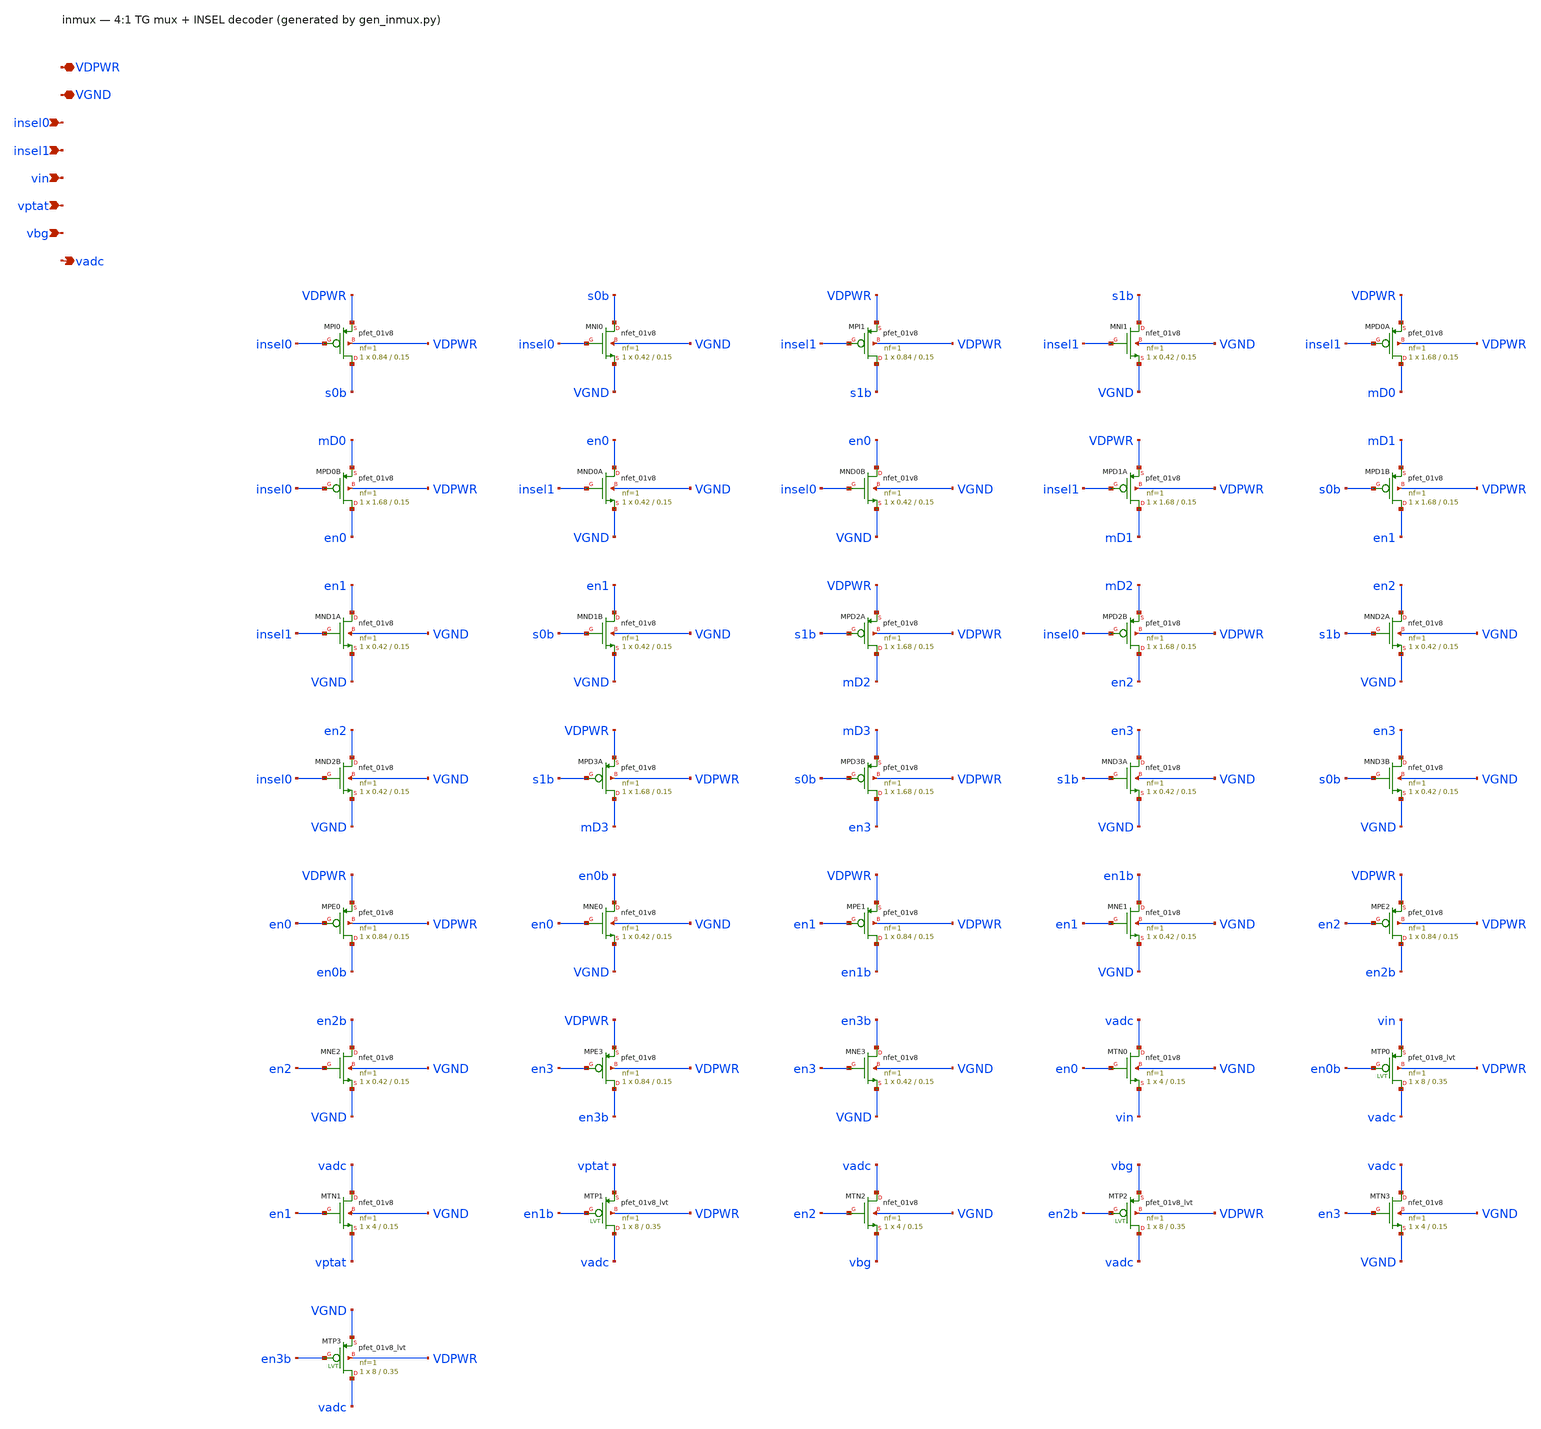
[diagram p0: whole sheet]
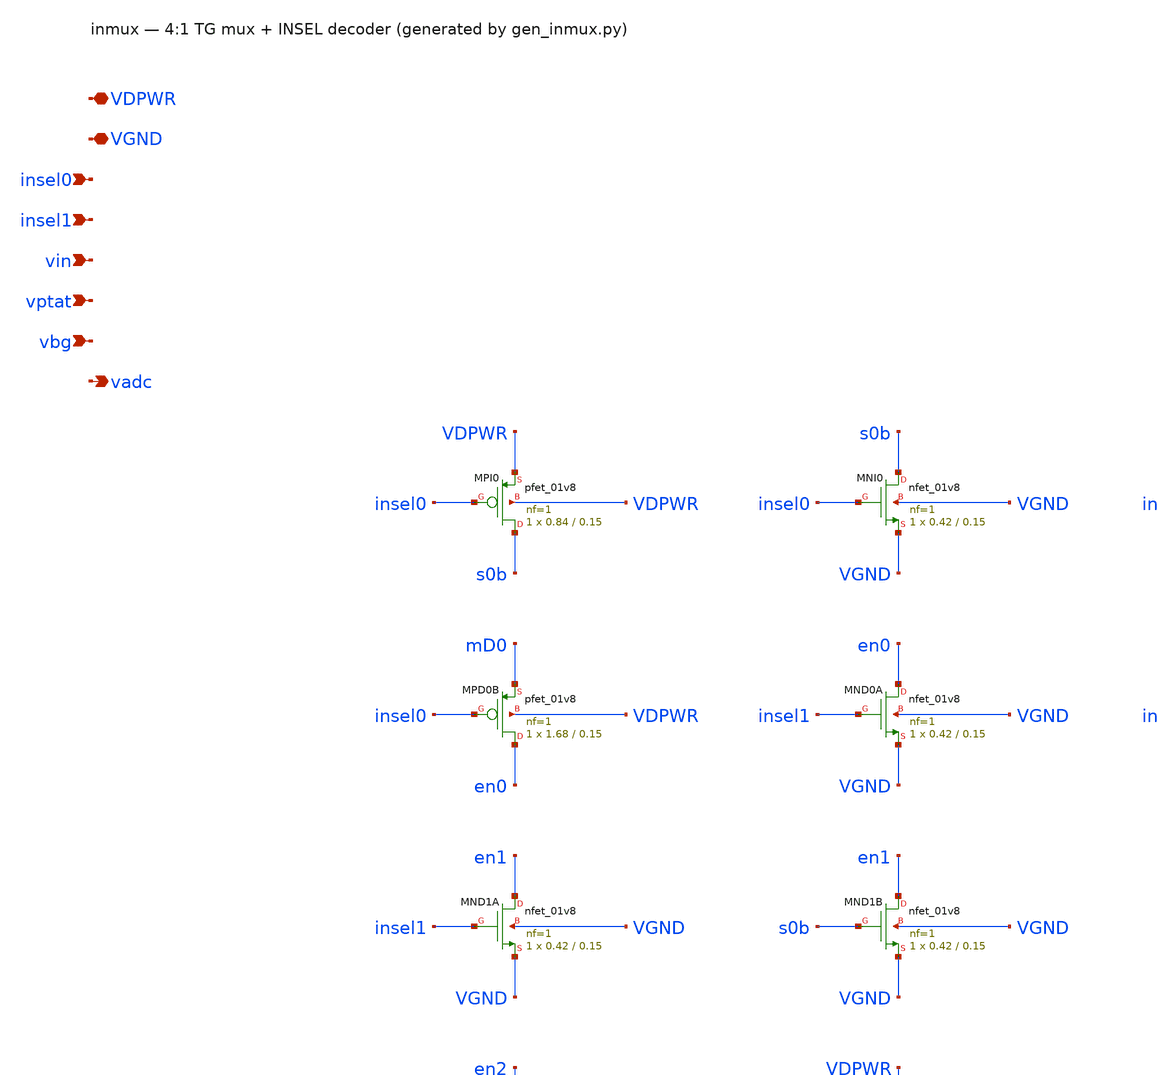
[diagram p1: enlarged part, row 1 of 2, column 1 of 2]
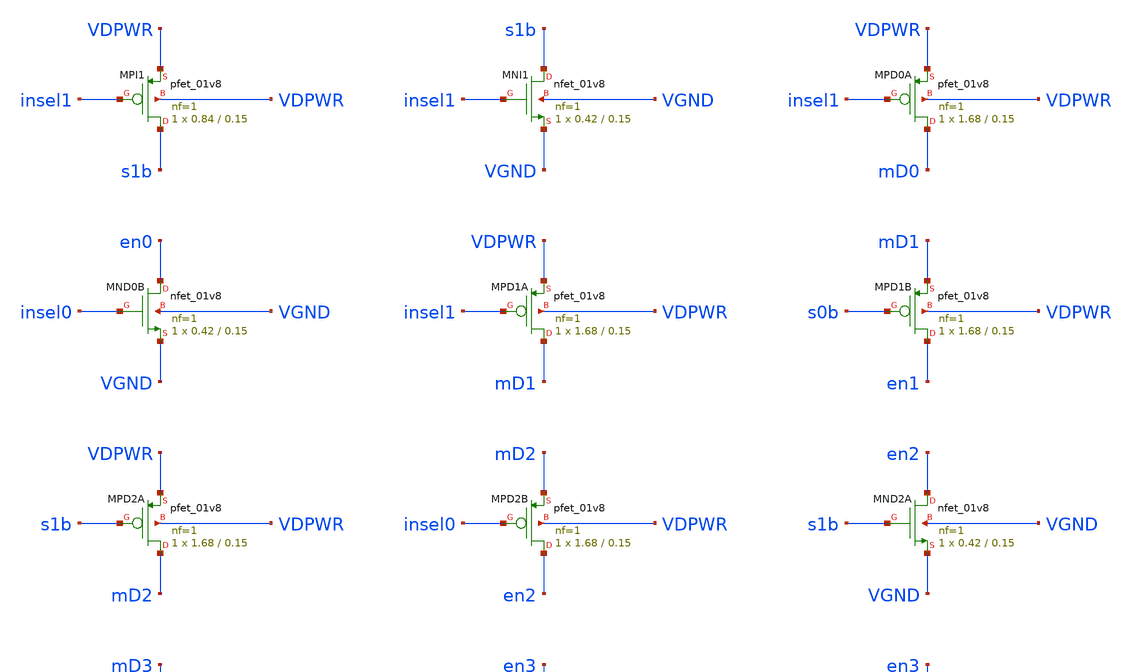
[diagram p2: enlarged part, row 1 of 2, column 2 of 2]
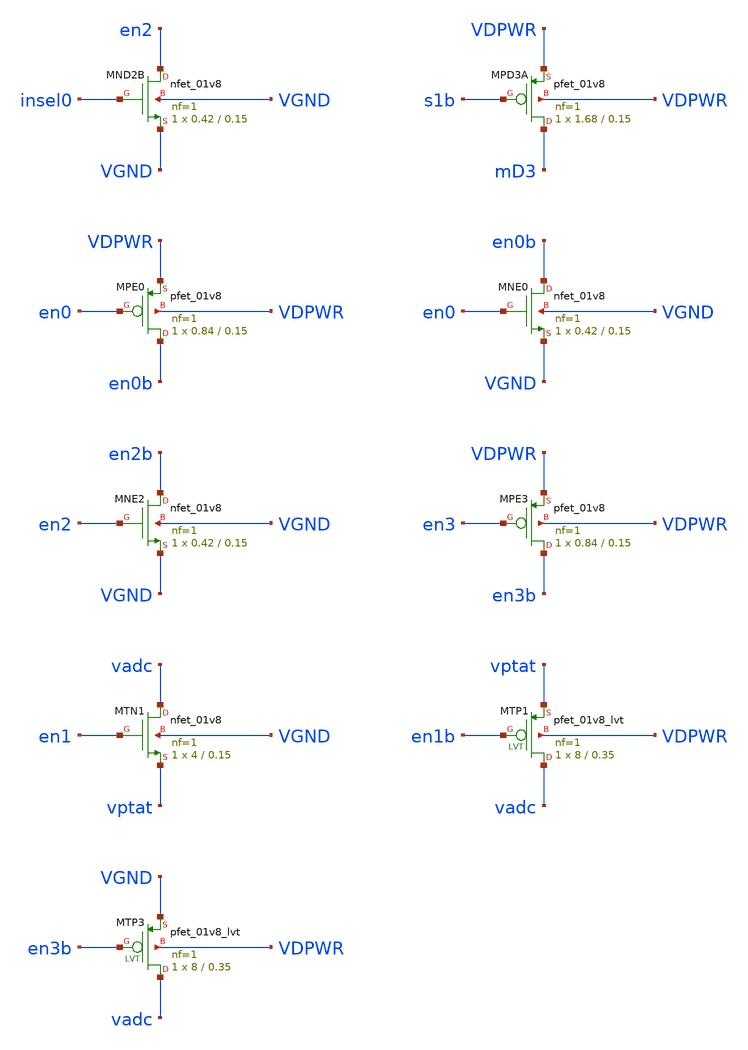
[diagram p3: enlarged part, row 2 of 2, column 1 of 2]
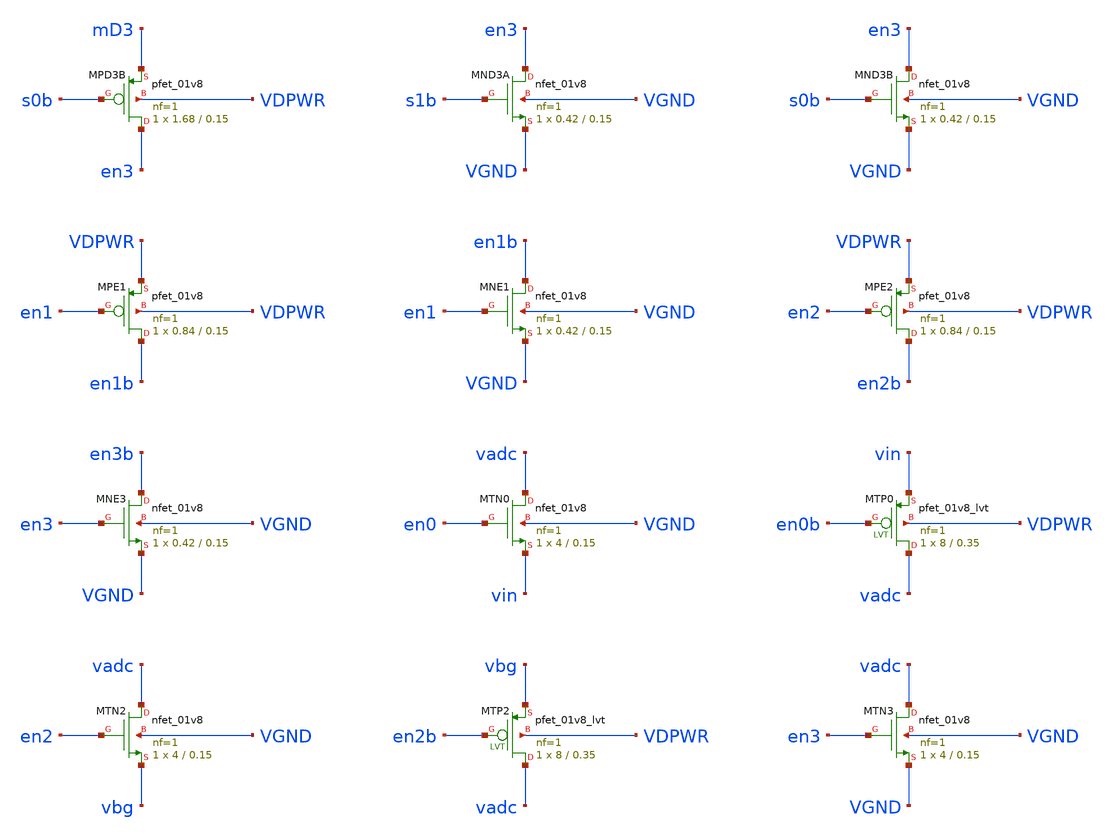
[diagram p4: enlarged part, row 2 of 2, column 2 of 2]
** sch_path: xschem/inmux.sch
**.subckt inmux VDPWR VGND insel0 insel1 vin vptat vbg vadc
*.iopin VDPWR
*.iopin VGND
*.ipin insel0
*.ipin insel1
*.ipin vin
*.ipin vptat
*.ipin vbg
*.opin vadc
XMPI0 s0b insel0 VDPWR VDPWR sky130_fd_pr__pfet_01v8 L=0.15 W=0.84 nf=1 ad='int((nf+1)/2) * W/nf * 0.29'
+ as='int((nf+2)/2) * W/nf * 0.29' pd='2*int((nf+1)/2) * (W/nf + 0.29)' ps='2*int((nf+2)/2) * (W/nf + 0.29)'
+ nrd='0.29 / W' nrs='0.29 / W' sa=0 sb=0 sd=0 mult=1 m=1
XMNI0 s0b insel0 VGND VGND sky130_fd_pr__nfet_01v8 L=0.15 W=0.42 nf=1 ad='int((1 + 1)/2) * 0.42 / 1 * 0.29'
+ as='int((1 + 2)/2) * 0.42 / 1 * 0.29' pd='2*int((1 + 1)/2) * (0.42 / 1 + 0.29)' ps='2*int((1 + 2)/2) * (0.42 / 1 + 0.29)'
+ nrd='0.29 / 0.42 ' nrs='0.29 / 0.42 ' sa=0 sb=0 sd=0 mult=1 m=1
XMPI1 s1b insel1 VDPWR VDPWR sky130_fd_pr__pfet_01v8 L=0.15 W=0.84 nf=1 ad='int((nf+1)/2) * W/nf * 0.29'
+ as='int((nf+2)/2) * W/nf * 0.29' pd='2*int((nf+1)/2) * (W/nf + 0.29)' ps='2*int((nf+2)/2) * (W/nf + 0.29)'
+ nrd='0.29 / W' nrs='0.29 / W' sa=0 sb=0 sd=0 mult=1 m=1
XMNI1 s1b insel1 VGND VGND sky130_fd_pr__nfet_01v8 L=0.15 W=0.42 nf=1 ad='int((1 + 1)/2) * 0.42 / 1 * 0.29'
+ as='int((1 + 2)/2) * 0.42 / 1 * 0.29' pd='2*int((1 + 1)/2) * (0.42 / 1 + 0.29)' ps='2*int((1 + 2)/2) * (0.42 / 1 + 0.29)'
+ nrd='0.29 / 0.42 ' nrs='0.29 / 0.42 ' sa=0 sb=0 sd=0 mult=1 m=1
XMPD0A mD0 insel1 VDPWR VDPWR sky130_fd_pr__pfet_01v8 L=0.15 W=1.68 nf=1 ad='int((nf+1)/2) * W/nf * 0.29'
+ as='int((nf+2)/2) * W/nf * 0.29' pd='2*int((nf+1)/2) * (W/nf + 0.29)' ps='2*int((nf+2)/2) * (W/nf + 0.29)'
+ nrd='0.29 / W' nrs='0.29 / W' sa=0 sb=0 sd=0 mult=1 m=1
XMPD0B en0 insel0 mD0 VDPWR sky130_fd_pr__pfet_01v8 L=0.15 W=1.68 nf=1 ad='int((nf+1)/2) * W/nf * 0.29'
+ as='int((nf+2)/2) * W/nf * 0.29' pd='2*int((nf+1)/2) * (W/nf + 0.29)' ps='2*int((nf+2)/2) * (W/nf + 0.29)'
+ nrd='0.29 / W' nrs='0.29 / W' sa=0 sb=0 sd=0 mult=1 m=1
XMND0A en0 insel1 VGND VGND sky130_fd_pr__nfet_01v8 L=0.15 W=0.42 nf=1 ad='int((1 + 1)/2) * 0.42 / 1 * 0.29'
+ as='int((1 + 2)/2) * 0.42 / 1 * 0.29' pd='2*int((1 + 1)/2) * (0.42 / 1 + 0.29)' ps='2*int((1 + 2)/2) * (0.42 / 1 + 0.29)'
+ nrd='0.29 / 0.42 ' nrs='0.29 / 0.42 ' sa=0 sb=0 sd=0 mult=1 m=1
XMND0B en0 insel0 VGND VGND sky130_fd_pr__nfet_01v8 L=0.15 W=0.42 nf=1 ad='int((1 + 1)/2) * 0.42 / 1 * 0.29'
+ as='int((1 + 2)/2) * 0.42 / 1 * 0.29' pd='2*int((1 + 1)/2) * (0.42 / 1 + 0.29)' ps='2*int((1 + 2)/2) * (0.42 / 1 + 0.29)'
+ nrd='0.29 / 0.42 ' nrs='0.29 / 0.42 ' sa=0 sb=0 sd=0 mult=1 m=1
XMPD1A mD1 insel1 VDPWR VDPWR sky130_fd_pr__pfet_01v8 L=0.15 W=1.68 nf=1 ad='int((nf+1)/2) * W/nf * 0.29'
+ as='int((nf+2)/2) * W/nf * 0.29' pd='2*int((nf+1)/2) * (W/nf + 0.29)' ps='2*int((nf+2)/2) * (W/nf + 0.29)'
+ nrd='0.29 / W' nrs='0.29 / W' sa=0 sb=0 sd=0 mult=1 m=1
XMPD1B en1 s0b mD1 VDPWR sky130_fd_pr__pfet_01v8 L=0.15 W=1.68 nf=1 ad='int((nf+1)/2) * W/nf * 0.29'
+ as='int((nf+2)/2) * W/nf * 0.29' pd='2*int((nf+1)/2) * (W/nf + 0.29)' ps='2*int((nf+2)/2) * (W/nf + 0.29)'
+ nrd='0.29 / W' nrs='0.29 / W' sa=0 sb=0 sd=0 mult=1 m=1
XMND1A en1 insel1 VGND VGND sky130_fd_pr__nfet_01v8 L=0.15 W=0.42 nf=1 ad='int((1 + 1)/2) * 0.42 / 1 * 0.29'
+ as='int((1 + 2)/2) * 0.42 / 1 * 0.29' pd='2*int((1 + 1)/2) * (0.42 / 1 + 0.29)' ps='2*int((1 + 2)/2) * (0.42 / 1 + 0.29)'
+ nrd='0.29 / 0.42 ' nrs='0.29 / 0.42 ' sa=0 sb=0 sd=0 mult=1 m=1
XMND1B en1 s0b VGND VGND sky130_fd_pr__nfet_01v8 L=0.15 W=0.42 nf=1 ad='int((1 + 1)/2) * 0.42 / 1 * 0.29'
+ as='int((1 + 2)/2) * 0.42 / 1 * 0.29' pd='2*int((1 + 1)/2) * (0.42 / 1 + 0.29)' ps='2*int((1 + 2)/2) * (0.42 / 1 + 0.29)'
+ nrd='0.29 / 0.42 ' nrs='0.29 / 0.42 ' sa=0 sb=0 sd=0 mult=1 m=1
XMPD2A mD2 s1b VDPWR VDPWR sky130_fd_pr__pfet_01v8 L=0.15 W=1.68 nf=1 ad='int((nf+1)/2) * W/nf * 0.29'
+ as='int((nf+2)/2) * W/nf * 0.29' pd='2*int((nf+1)/2) * (W/nf + 0.29)' ps='2*int((nf+2)/2) * (W/nf + 0.29)'
+ nrd='0.29 / W' nrs='0.29 / W' sa=0 sb=0 sd=0 mult=1 m=1
XMPD2B en2 insel0 mD2 VDPWR sky130_fd_pr__pfet_01v8 L=0.15 W=1.68 nf=1 ad='int((nf+1)/2) * W/nf * 0.29'
+ as='int((nf+2)/2) * W/nf * 0.29' pd='2*int((nf+1)/2) * (W/nf + 0.29)' ps='2*int((nf+2)/2) * (W/nf + 0.29)'
+ nrd='0.29 / W' nrs='0.29 / W' sa=0 sb=0 sd=0 mult=1 m=1
XMND2A en2 s1b VGND VGND sky130_fd_pr__nfet_01v8 L=0.15 W=0.42 nf=1 ad='int((1 + 1)/2) * 0.42 / 1 * 0.29'
+ as='int((1 + 2)/2) * 0.42 / 1 * 0.29' pd='2*int((1 + 1)/2) * (0.42 / 1 + 0.29)' ps='2*int((1 + 2)/2) * (0.42 / 1 + 0.29)'
+ nrd='0.29 / 0.42 ' nrs='0.29 / 0.42 ' sa=0 sb=0 sd=0 mult=1 m=1
XMND2B en2 insel0 VGND VGND sky130_fd_pr__nfet_01v8 L=0.15 W=0.42 nf=1 ad='int((1 + 1)/2) * 0.42 / 1 * 0.29'
+ as='int((1 + 2)/2) * 0.42 / 1 * 0.29' pd='2*int((1 + 1)/2) * (0.42 / 1 + 0.29)' ps='2*int((1 + 2)/2) * (0.42 / 1 + 0.29)'
+ nrd='0.29 / 0.42 ' nrs='0.29 / 0.42 ' sa=0 sb=0 sd=0 mult=1 m=1
XMPD3A mD3 s1b VDPWR VDPWR sky130_fd_pr__pfet_01v8 L=0.15 W=1.68 nf=1 ad='int((nf+1)/2) * W/nf * 0.29'
+ as='int((nf+2)/2) * W/nf * 0.29' pd='2*int((nf+1)/2) * (W/nf + 0.29)' ps='2*int((nf+2)/2) * (W/nf + 0.29)'
+ nrd='0.29 / W' nrs='0.29 / W' sa=0 sb=0 sd=0 mult=1 m=1
XMPD3B en3 s0b mD3 VDPWR sky130_fd_pr__pfet_01v8 L=0.15 W=1.68 nf=1 ad='int((nf+1)/2) * W/nf * 0.29'
+ as='int((nf+2)/2) * W/nf * 0.29' pd='2*int((nf+1)/2) * (W/nf + 0.29)' ps='2*int((nf+2)/2) * (W/nf + 0.29)'
+ nrd='0.29 / W' nrs='0.29 / W' sa=0 sb=0 sd=0 mult=1 m=1
XMND3A en3 s1b VGND VGND sky130_fd_pr__nfet_01v8 L=0.15 W=0.42 nf=1 ad='int((1 + 1)/2) * 0.42 / 1 * 0.29'
+ as='int((1 + 2)/2) * 0.42 / 1 * 0.29' pd='2*int((1 + 1)/2) * (0.42 / 1 + 0.29)' ps='2*int((1 + 2)/2) * (0.42 / 1 + 0.29)'
+ nrd='0.29 / 0.42 ' nrs='0.29 / 0.42 ' sa=0 sb=0 sd=0 mult=1 m=1
XMND3B en3 s0b VGND VGND sky130_fd_pr__nfet_01v8 L=0.15 W=0.42 nf=1 ad='int((1 + 1)/2) * 0.42 / 1 * 0.29'
+ as='int((1 + 2)/2) * 0.42 / 1 * 0.29' pd='2*int((1 + 1)/2) * (0.42 / 1 + 0.29)' ps='2*int((1 + 2)/2) * (0.42 / 1 + 0.29)'
+ nrd='0.29 / 0.42 ' nrs='0.29 / 0.42 ' sa=0 sb=0 sd=0 mult=1 m=1
XMPE0 en0b en0 VDPWR VDPWR sky130_fd_pr__pfet_01v8 L=0.15 W=0.84 nf=1 ad='int((nf+1)/2) * W/nf * 0.29'
+ as='int((nf+2)/2) * W/nf * 0.29' pd='2*int((nf+1)/2) * (W/nf + 0.29)' ps='2*int((nf+2)/2) * (W/nf + 0.29)'
+ nrd='0.29 / W' nrs='0.29 / W' sa=0 sb=0 sd=0 mult=1 m=1
XMNE0 en0b en0 VGND VGND sky130_fd_pr__nfet_01v8 L=0.15 W=0.42 nf=1 ad='int((1 + 1)/2) * 0.42 / 1 * 0.29'
+ as='int((1 + 2)/2) * 0.42 / 1 * 0.29' pd='2*int((1 + 1)/2) * (0.42 / 1 + 0.29)' ps='2*int((1 + 2)/2) * (0.42 / 1 + 0.29)'
+ nrd='0.29 / 0.42 ' nrs='0.29 / 0.42 ' sa=0 sb=0 sd=0 mult=1 m=1
XMPE1 en1b en1 VDPWR VDPWR sky130_fd_pr__pfet_01v8 L=0.15 W=0.84 nf=1 ad='int((nf+1)/2) * W/nf * 0.29'
+ as='int((nf+2)/2) * W/nf * 0.29' pd='2*int((nf+1)/2) * (W/nf + 0.29)' ps='2*int((nf+2)/2) * (W/nf + 0.29)'
+ nrd='0.29 / W' nrs='0.29 / W' sa=0 sb=0 sd=0 mult=1 m=1
XMNE1 en1b en1 VGND VGND sky130_fd_pr__nfet_01v8 L=0.15 W=0.42 nf=1 ad='int((1 + 1)/2) * 0.42 / 1 * 0.29'
+ as='int((1 + 2)/2) * 0.42 / 1 * 0.29' pd='2*int((1 + 1)/2) * (0.42 / 1 + 0.29)' ps='2*int((1 + 2)/2) * (0.42 / 1 + 0.29)'
+ nrd='0.29 / 0.42 ' nrs='0.29 / 0.42 ' sa=0 sb=0 sd=0 mult=1 m=1
XMPE2 en2b en2 VDPWR VDPWR sky130_fd_pr__pfet_01v8 L=0.15 W=0.84 nf=1 ad='int((nf+1)/2) * W/nf * 0.29'
+ as='int((nf+2)/2) * W/nf * 0.29' pd='2*int((nf+1)/2) * (W/nf + 0.29)' ps='2*int((nf+2)/2) * (W/nf + 0.29)'
+ nrd='0.29 / W' nrs='0.29 / W' sa=0 sb=0 sd=0 mult=1 m=1
XMNE2 en2b en2 VGND VGND sky130_fd_pr__nfet_01v8 L=0.15 W=0.42 nf=1 ad='int((1 + 1)/2) * 0.42 / 1 * 0.29'
+ as='int((1 + 2)/2) * 0.42 / 1 * 0.29' pd='2*int((1 + 1)/2) * (0.42 / 1 + 0.29)' ps='2*int((1 + 2)/2) * (0.42 / 1 + 0.29)'
+ nrd='0.29 / 0.42 ' nrs='0.29 / 0.42 ' sa=0 sb=0 sd=0 mult=1 m=1
XMPE3 en3b en3 VDPWR VDPWR sky130_fd_pr__pfet_01v8 L=0.15 W=0.84 nf=1 ad='int((nf+1)/2) * W/nf * 0.29'
+ as='int((nf+2)/2) * W/nf * 0.29' pd='2*int((nf+1)/2) * (W/nf + 0.29)' ps='2*int((nf+2)/2) * (W/nf + 0.29)'
+ nrd='0.29 / W' nrs='0.29 / W' sa=0 sb=0 sd=0 mult=1 m=1
XMNE3 en3b en3 VGND VGND sky130_fd_pr__nfet_01v8 L=0.15 W=0.42 nf=1 ad='int((1 + 1)/2) * 0.42 / 1 * 0.29'
+ as='int((1 + 2)/2) * 0.42 / 1 * 0.29' pd='2*int((1 + 1)/2) * (0.42 / 1 + 0.29)' ps='2*int((1 + 2)/2) * (0.42 / 1 + 0.29)'
+ nrd='0.29 / 0.42 ' nrs='0.29 / 0.42 ' sa=0 sb=0 sd=0 mult=1 m=1
XMTN0 vadc en0 vin VGND sky130_fd_pr__nfet_01v8 L=0.15 W=4 nf=1 ad='int((1 + 1)/2) * 4 / 1 * 0.29' as='int((1 + 2)/2) * 4 / 1 * 0.29'
+ pd='2*int((1 + 1)/2) * (4 / 1 + 0.29)' ps='2*int((1 + 2)/2) * (4 / 1 + 0.29)' nrd='0.29 / 4 ' nrs='0.29 / 4 '
+ sa=0 sb=0 sd=0 mult=1 m=1
XMTP0 vadc en0b vin VDPWR sky130_fd_pr__pfet_01v8_lvt L=0.35 W=8 nf=1 ad='int((1 + 1)/2) * 8 / 1 * 0.29'
+ as='int((1 + 2)/2) * 8 / 1 * 0.29' pd='2*int((1 + 1)/2) * (8 / 1 + 0.29)' ps='2*int((1 + 2)/2) * (8 / 1 + 0.29)'
+ nrd='0.29 / 8 ' nrs='0.29 / 8 ' sa=0 sb=0 sd=0 mult=1 m=1
XMTN1 vadc en1 vptat VGND sky130_fd_pr__nfet_01v8 L=0.15 W=4 nf=1 ad='int((1 + 1)/2) * 4 / 1 * 0.29'
+ as='int((1 + 2)/2) * 4 / 1 * 0.29' pd='2*int((1 + 1)/2) * (4 / 1 + 0.29)' ps='2*int((1 + 2)/2) * (4 / 1 + 0.29)'
+ nrd='0.29 / 4 ' nrs='0.29 / 4 ' sa=0 sb=0 sd=0 mult=1 m=1
XMTP1 vadc en1b vptat VDPWR sky130_fd_pr__pfet_01v8_lvt L=0.35 W=8 nf=1 ad='int((1 + 1)/2) * 8 / 1 * 0.29'
+ as='int((1 + 2)/2) * 8 / 1 * 0.29' pd='2*int((1 + 1)/2) * (8 / 1 + 0.29)' ps='2*int((1 + 2)/2) * (8 / 1 + 0.29)'
+ nrd='0.29 / 8 ' nrs='0.29 / 8 ' sa=0 sb=0 sd=0 mult=1 m=1
XMTN2 vadc en2 vbg VGND sky130_fd_pr__nfet_01v8 L=0.15 W=4 nf=1 ad='int((1 + 1)/2) * 4 / 1 * 0.29' as='int((1 + 2)/2) * 4 / 1 * 0.29'
+ pd='2*int((1 + 1)/2) * (4 / 1 + 0.29)' ps='2*int((1 + 2)/2) * (4 / 1 + 0.29)' nrd='0.29 / 4 ' nrs='0.29 / 4 '
+ sa=0 sb=0 sd=0 mult=1 m=1
XMTP2 vadc en2b vbg VDPWR sky130_fd_pr__pfet_01v8_lvt L=0.35 W=8 nf=1 ad='int((1 + 1)/2) * 8 / 1 * 0.29'
+ as='int((1 + 2)/2) * 8 / 1 * 0.29' pd='2*int((1 + 1)/2) * (8 / 1 + 0.29)' ps='2*int((1 + 2)/2) * (8 / 1 + 0.29)'
+ nrd='0.29 / 8 ' nrs='0.29 / 8 ' sa=0 sb=0 sd=0 mult=1 m=1
XMTN3 vadc en3 VGND VGND sky130_fd_pr__nfet_01v8 L=0.15 W=4 nf=1 ad='int((1 + 1)/2) * 4 / 1 * 0.29' as='int((1 + 2)/2) * 4 / 1 * 0.29'
+ pd='2*int((1 + 1)/2) * (4 / 1 + 0.29)' ps='2*int((1 + 2)/2) * (4 / 1 + 0.29)' nrd='0.29 / 4 ' nrs='0.29 / 4 '
+ sa=0 sb=0 sd=0 mult=1 m=1
XMTP3 vadc en3b VGND VDPWR sky130_fd_pr__pfet_01v8_lvt L=0.35 W=8 nf=1 ad='int((1 + 1)/2) * 8 / 1 * 0.29'
+ as='int((1 + 2)/2) * 8 / 1 * 0.29' pd='2*int((1 + 1)/2) * (8 / 1 + 0.29)' ps='2*int((1 + 2)/2) * (8 / 1 + 0.29)'
+ nrd='0.29 / 8 ' nrs='0.29 / 8 ' sa=0 sb=0 sd=0 mult=1 m=1
**.ends
.end
